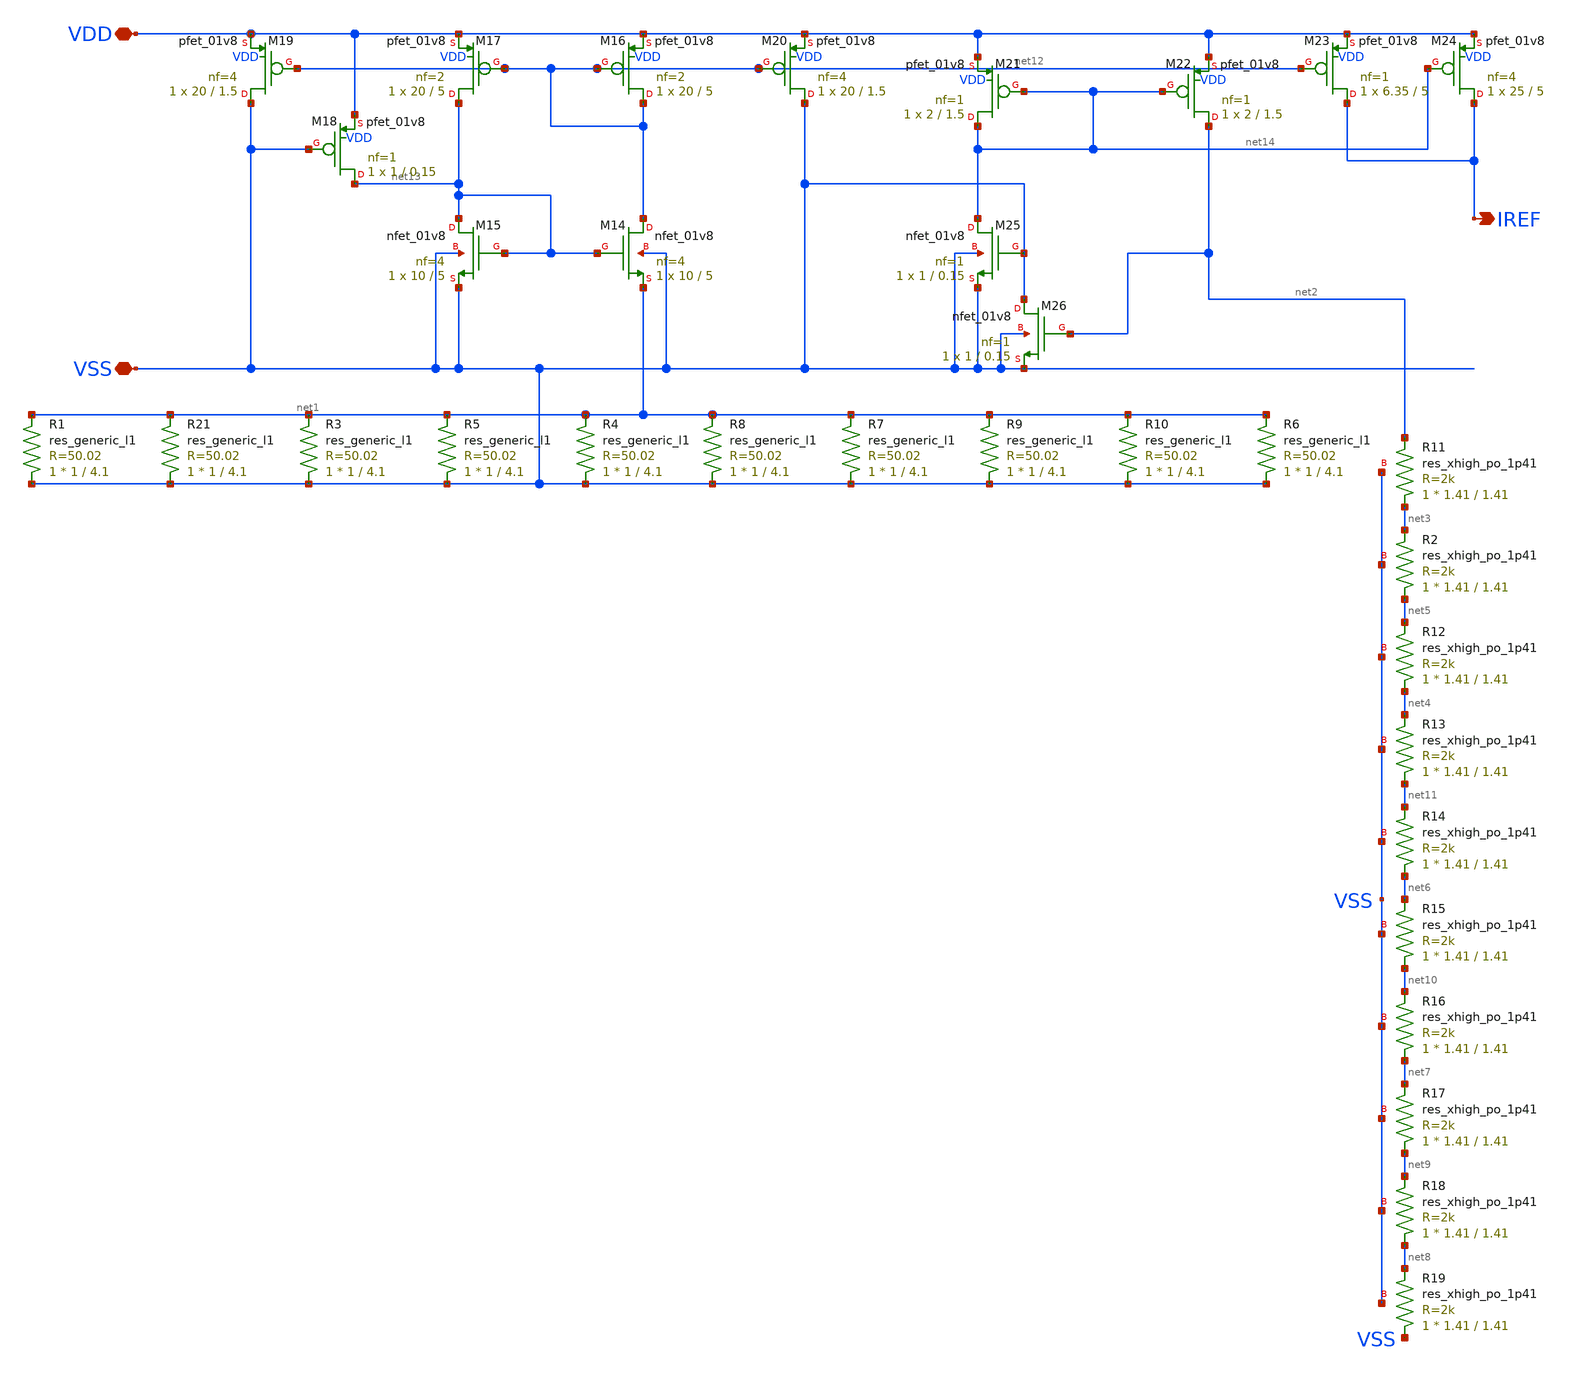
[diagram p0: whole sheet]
** sch_path: bandgap/bgr/current-mode-bgr.sch
**.subckt current-mode-bgr IREF VDD VSS
*.opin IREF
*.iopin VDD
*.iopin VSS
R21 VSS net1 sky130_fd_pr__res_generic_l1 W=1 L=4.1 m=1
R1 VSS net1 sky130_fd_pr__res_generic_l1 W=1 L=4.1 m=1
R3 VSS net1 sky130_fd_pr__res_generic_l1 W=1 L=4.1 m=1
R4 VSS net1 sky130_fd_pr__res_generic_l1 W=1 L=4.1 m=1
R5 VSS net1 sky130_fd_pr__res_generic_l1 W=1 L=4.1 m=1
R6 VSS net1 sky130_fd_pr__res_generic_l1 W=1 L=4.1 m=1
R7 VSS net1 sky130_fd_pr__res_generic_l1 W=1 L=4.1 m=1
R8 VSS net1 sky130_fd_pr__res_generic_l1 W=1 L=4.1 m=1
R9 VSS net1 sky130_fd_pr__res_generic_l1 W=1 L=4.1 m=1
R10 VSS net1 sky130_fd_pr__res_generic_l1 W=1 L=4.1 m=1
XR11 net3 net2 VSS sky130_fd_pr__res_xhigh_po_1p41 L=1.41 mult=1 m=1
XR2 net5 net3 VSS sky130_fd_pr__res_xhigh_po_1p41 L=1.41 mult=1 m=1
XR12 net4 net5 VSS sky130_fd_pr__res_xhigh_po_1p41 L=1.41 mult=1 m=1
XR13 net11 net4 VSS sky130_fd_pr__res_xhigh_po_1p41 L=1.41 mult=1 m=1
XR14 net6 net11 VSS sky130_fd_pr__res_xhigh_po_1p41 L=1.41 mult=1 m=1
XR15 net10 net6 VSS sky130_fd_pr__res_xhigh_po_1p41 L=1.41 mult=1 m=1
XR16 net7 net10 VSS sky130_fd_pr__res_xhigh_po_1p41 L=1.41 mult=1 m=1
XR17 net9 net7 VSS sky130_fd_pr__res_xhigh_po_1p41 L=1.41 mult=1 m=1
XR18 net8 net9 VSS sky130_fd_pr__res_xhigh_po_1p41 L=1.41 mult=1 m=1
XR19 VSS net8 VSS sky130_fd_pr__res_xhigh_po_1p41 L=1.41 mult=1 m=1
XM14 net12 net13 net1 VSS sky130_fd_pr__nfet_01v8 L=5 W=10 nf=4 ad='int((nf+1)/2) * W/nf * 0.29' as='int((nf+2)/2) * W/nf * 0.29'
+ pd='2*int((nf+1)/2) * (W/nf + 0.29)' ps='2*int((nf+2)/2) * (W/nf + 0.29)' nrd='0.29 / W' nrs='0.29 / W'
+ sa=0 sb=0 sd=0 mult=1 m=1
XM15 net13 net13 VSS VSS sky130_fd_pr__nfet_01v8 L=5 W=10 nf=4 ad='int((nf+1)/2) * W/nf * 0.29' as='int((nf+2)/2) * W/nf * 0.29'
+ pd='2*int((nf+1)/2) * (W/nf + 0.29)' ps='2*int((nf+2)/2) * (W/nf + 0.29)' nrd='0.29 / W' nrs='0.29 / W'
+ sa=0 sb=0 sd=0 mult=1 m=1
XM16 net12 net12 VDD VDD sky130_fd_pr__pfet_01v8 L=5 W=20 nf=2 ad='int((nf+1)/2) * W/nf * 0.29' as='int((nf+2)/2) * W/nf * 0.29'
+ pd='2*int((nf+1)/2) * (W/nf + 0.29)' ps='2*int((nf+2)/2) * (W/nf + 0.29)' nrd='0.29 / W' nrs='0.29 / W'
+ sa=0 sb=0 sd=0 mult=1 m=1
XM17 net13 net12 VDD VDD sky130_fd_pr__pfet_01v8 L=5 W=20 nf=2 ad='int((nf+1)/2) * W/nf * 0.29' as='int((nf+2)/2) * W/nf * 0.29'
+ pd='2*int((nf+1)/2) * (W/nf + 0.29)' ps='2*int((nf+2)/2) * (W/nf + 0.29)' nrd='0.29 / W' nrs='0.29 / W'
+ sa=0 sb=0 sd=0 mult=1 m=1
XM18 net13 VSS VDD VDD sky130_fd_pr__pfet_01v8 L=0.15 W=1 nf=1 ad='int((nf+1)/2) * W/nf * 0.29' as='int((nf+2)/2) * W/nf * 0.29'
+ pd='2*int((nf+1)/2) * (W/nf + 0.29)' ps='2*int((nf+2)/2) * (W/nf + 0.29)' nrd='0.29 / W' nrs='0.29 / W'
+ sa=0 sb=0 sd=0 mult=1 m=1
XM19 VSS net12 VDD VDD sky130_fd_pr__pfet_01v8 L=1.5 W=20 nf=4 ad='int((nf+1)/2) * W/nf * 0.29' as='int((nf+2)/2) * W/nf * 0.29'
+ pd='2*int((nf+1)/2) * (W/nf + 0.29)' ps='2*int((nf+2)/2) * (W/nf + 0.29)' nrd='0.29 / W' nrs='0.29 / W'
+ sa=0 sb=0 sd=0 mult=1 m=1
XM20 VSS net12 VDD VDD sky130_fd_pr__pfet_01v8 L=1.5 W=20 nf=4 ad='int((nf+1)/2) * W/nf * 0.29' as='int((nf+2)/2) * W/nf * 0.29'
+ pd='2*int((nf+1)/2) * (W/nf + 0.29)' ps='2*int((nf+2)/2) * (W/nf + 0.29)' nrd='0.29 / W' nrs='0.29 / W'
+ sa=0 sb=0 sd=0 mult=1 m=1
XM21 net14 net14 VDD VDD sky130_fd_pr__pfet_01v8 L=1.5 W=2 nf=1 ad='int((nf+1)/2) * W/nf * 0.29' as='int((nf+2)/2) * W/nf * 0.29'
+ pd='2*int((nf+1)/2) * (W/nf + 0.29)' ps='2*int((nf+2)/2) * (W/nf + 0.29)' nrd='0.29 / W' nrs='0.29 / W'
+ sa=0 sb=0 sd=0 mult=1 m=1
XM22 net2 net14 VDD VDD sky130_fd_pr__pfet_01v8 L=1.5 W=2 nf=1 ad='int((nf+1)/2) * W/nf * 0.29' as='int((nf+2)/2) * W/nf * 0.29'
+ pd='2*int((nf+1)/2) * (W/nf + 0.29)' ps='2*int((nf+2)/2) * (W/nf + 0.29)' nrd='0.29 / W' nrs='0.29 / W'
+ sa=0 sb=0 sd=0 mult=1 m=1
XM23 IREF net12 VDD VDD sky130_fd_pr__pfet_01v8 L=5 W=6.35 nf=1 ad='int((nf+1)/2) * W/nf * 0.29' as='int((nf+2)/2) * W/nf * 0.29'
+ pd='2*int((nf+1)/2) * (W/nf + 0.29)' ps='2*int((nf+2)/2) * (W/nf + 0.29)' nrd='0.29 / W' nrs='0.29 / W'
+ sa=0 sb=0 sd=0 mult=1 m=1
XM24 IREF net14 VDD VDD sky130_fd_pr__pfet_01v8 L=5 W=25 nf=4 ad='int((nf+1)/2) * W/nf * 0.29' as='int((nf+2)/2) * W/nf * 0.29'
+ pd='2*int((nf+1)/2) * (W/nf + 0.29)' ps='2*int((nf+2)/2) * (W/nf + 0.29)' nrd='0.29 / W' nrs='0.29 / W'
+ sa=0 sb=0 sd=0 mult=1 m=1
XM25 net14 VSS VSS VSS sky130_fd_pr__nfet_01v8 L=0.15 W=1 nf=1 ad='int((nf+1)/2) * W/nf * 0.29' as='int((nf+2)/2) * W/nf * 0.29'
+ pd='2*int((nf+1)/2) * (W/nf + 0.29)' ps='2*int((nf+2)/2) * (W/nf + 0.29)' nrd='0.29 / W' nrs='0.29 / W'
+ sa=0 sb=0 sd=0 mult=1 m=1
XM26 VSS net2 VSS VSS sky130_fd_pr__nfet_01v8 L=0.15 W=1 nf=1 ad='int((nf+1)/2) * W/nf * 0.29' as='int((nf+2)/2) * W/nf * 0.29'
+ pd='2*int((nf+1)/2) * (W/nf + 0.29)' ps='2*int((nf+2)/2) * (W/nf + 0.29)' nrd='0.29 / W' nrs='0.29 / W'
+ sa=0 sb=0 sd=0 mult=1 m=1
**.ends
.end
